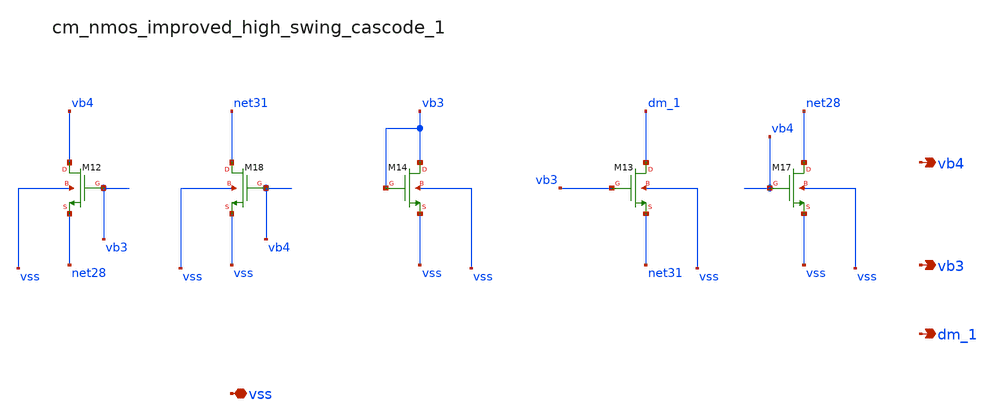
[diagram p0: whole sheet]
** sch_path: analog-db/raw/ldo_001_analoggym_basic/hier/blocks/cm_nmos_improved_high_swing_cascode_1.sch
**.subckt cm_nmos_improved_high_swing_cascode_1 vss vb4 vb3 dm_1
*.iopin vss
*.opin vb4
*.opin vb3
*.opin dm_1
XM12 vb4 vb3 net28 vss sg13_lv_nmos w=x_dut_xm12_w l=x_dut_xm12_l ng=1 m=x_dut_xm12_m
XM13 dm_1 vb3 net31 vss sg13_lv_nmos w=x_dut_xm13_w l=x_dut_xm13_l ng=1 m=x_dut_xm13_m
XM14 vb3 vb3 vss vss sg13_lv_nmos w=x_dut_xm14_w l=x_dut_xm14_l ng=1 m=x_dut_xm14_m
XM17 net28 vb4 vss vss sg13_lv_nmos w=x_dut_xm17_w l=x_dut_xm17_l ng=1 m=x_dut_xm17_m
XM18 net31 vb4 vss vss sg13_lv_nmos w=x_dut_xm18_w l=x_dut_xm18_l ng=1 m=x_dut_xm18_m
**.ends
.end
